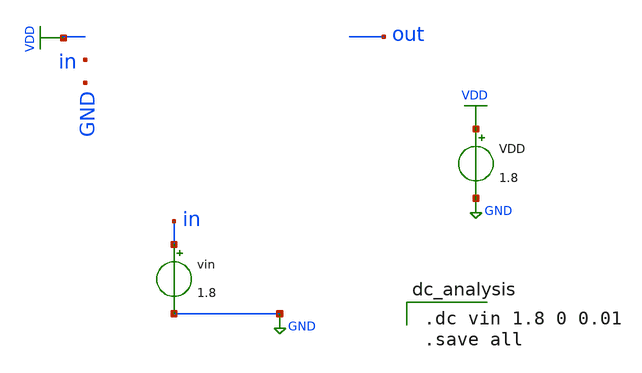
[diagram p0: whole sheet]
** sch_path: pll/dividers_lib/divider/xschem/inv_DC.sch
**.subckt inv_DC
vin in GND 1.8
VDD VDD GND 1.8
**** begin user architecture code

** opencircuitdesign pdks install
.lib $::SKYWATER_MODELS/sky130.lib.spice tt



.dc vin 1.8 0 0.01
.save all

**** end user architecture code
**.ends
.GLOBAL VDD
.GLOBAL GND
.end
